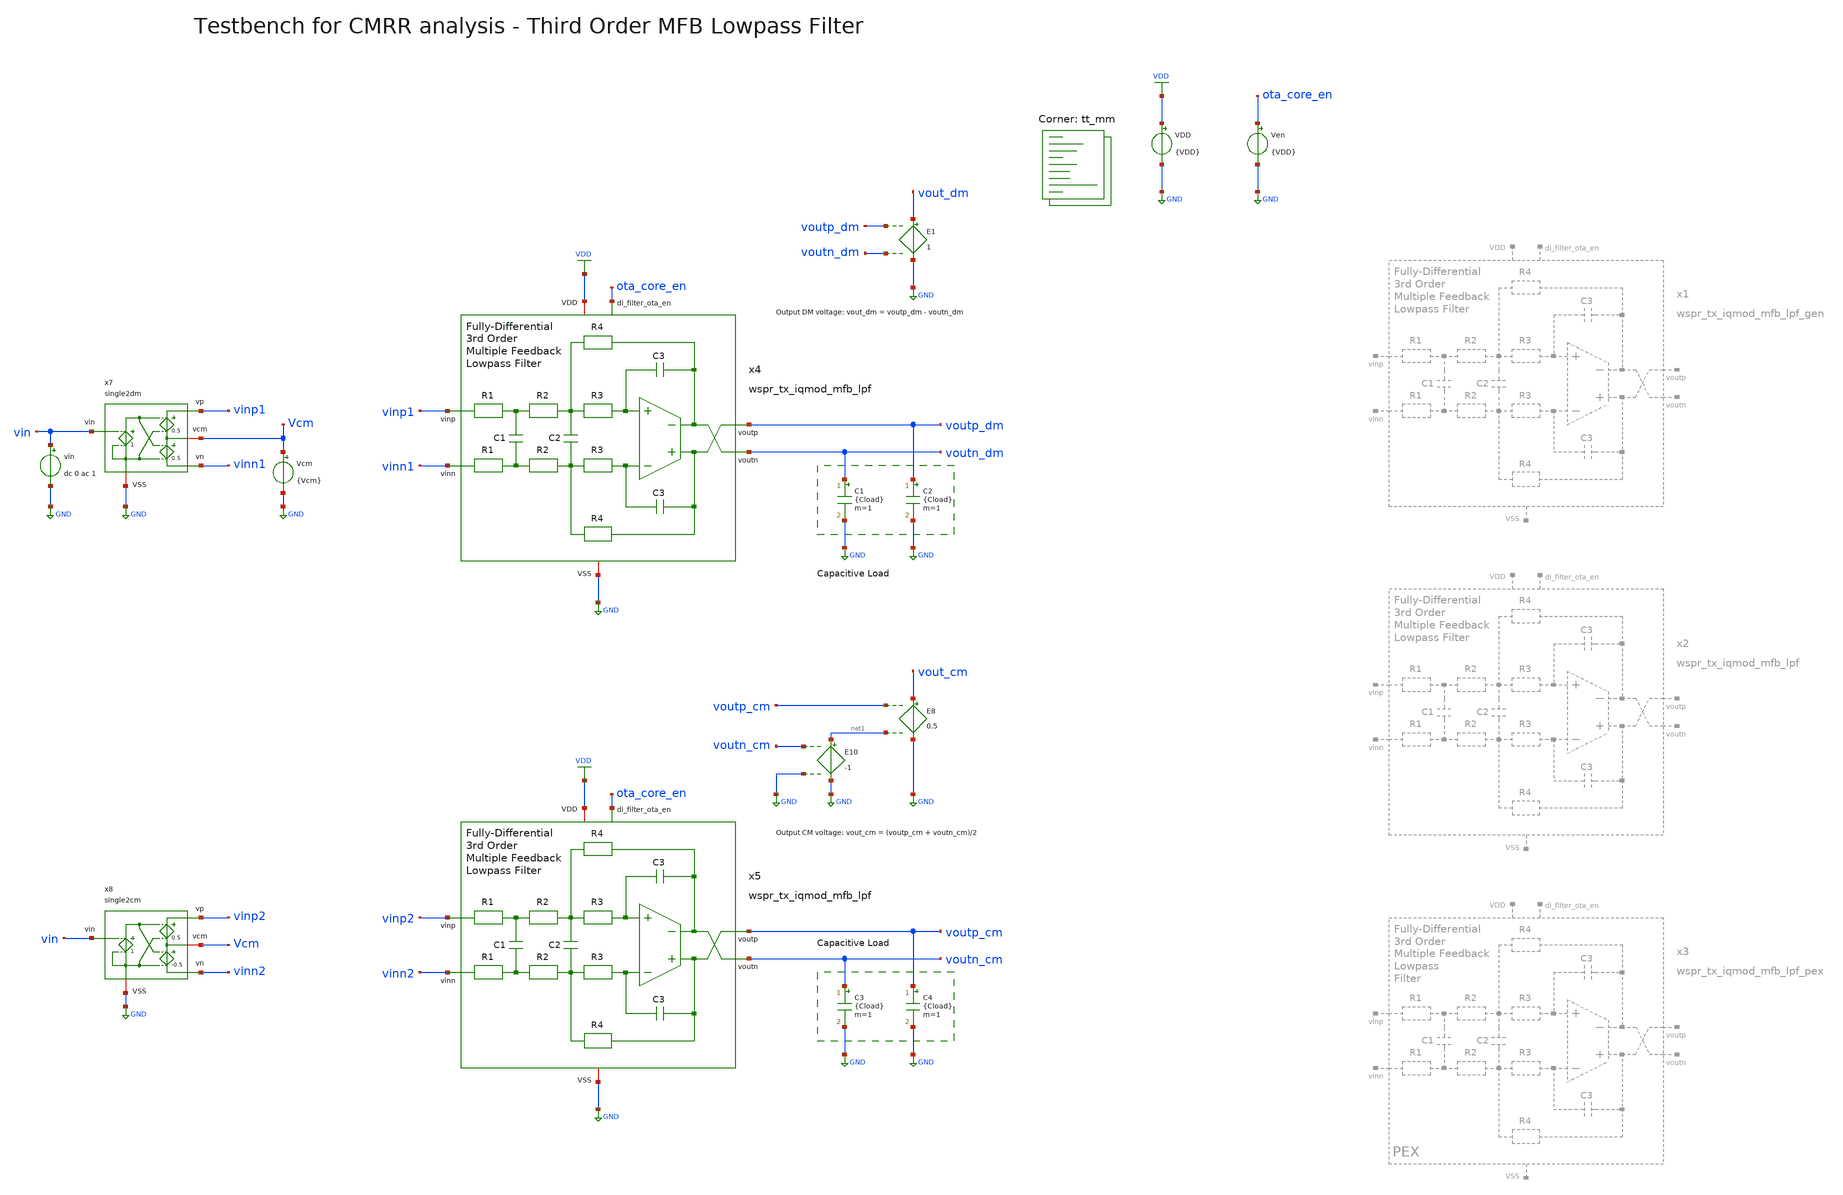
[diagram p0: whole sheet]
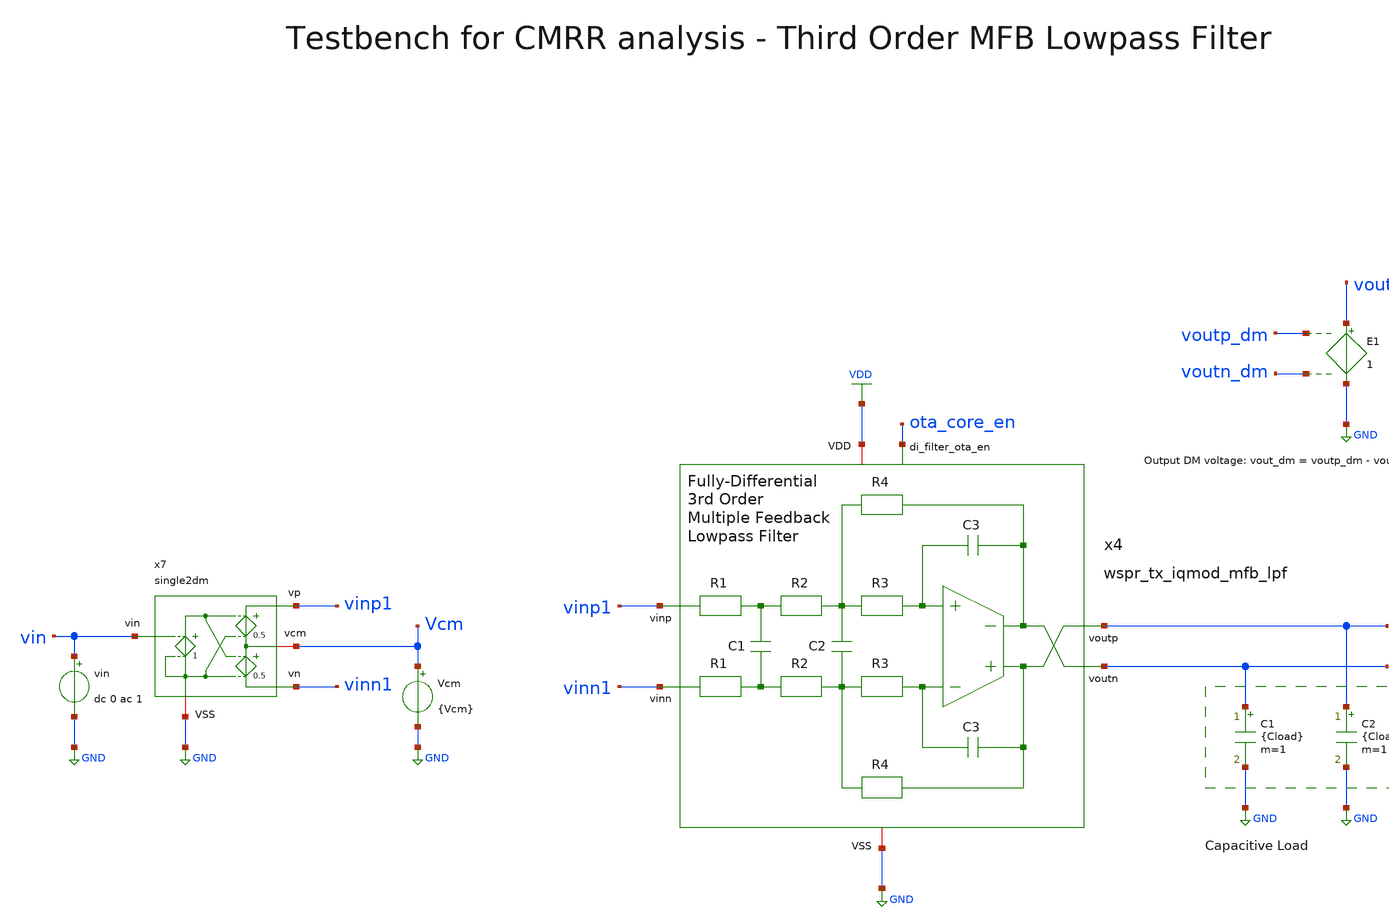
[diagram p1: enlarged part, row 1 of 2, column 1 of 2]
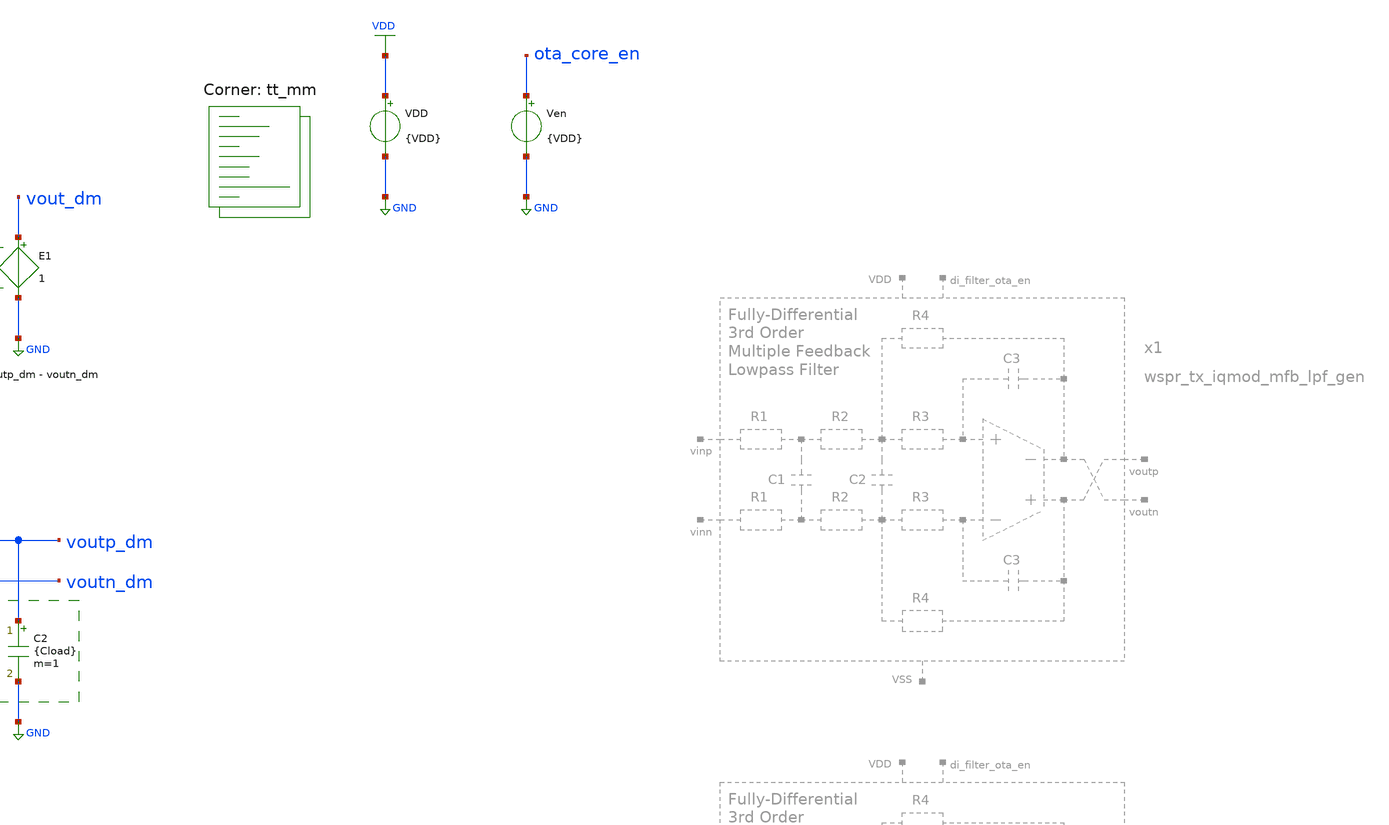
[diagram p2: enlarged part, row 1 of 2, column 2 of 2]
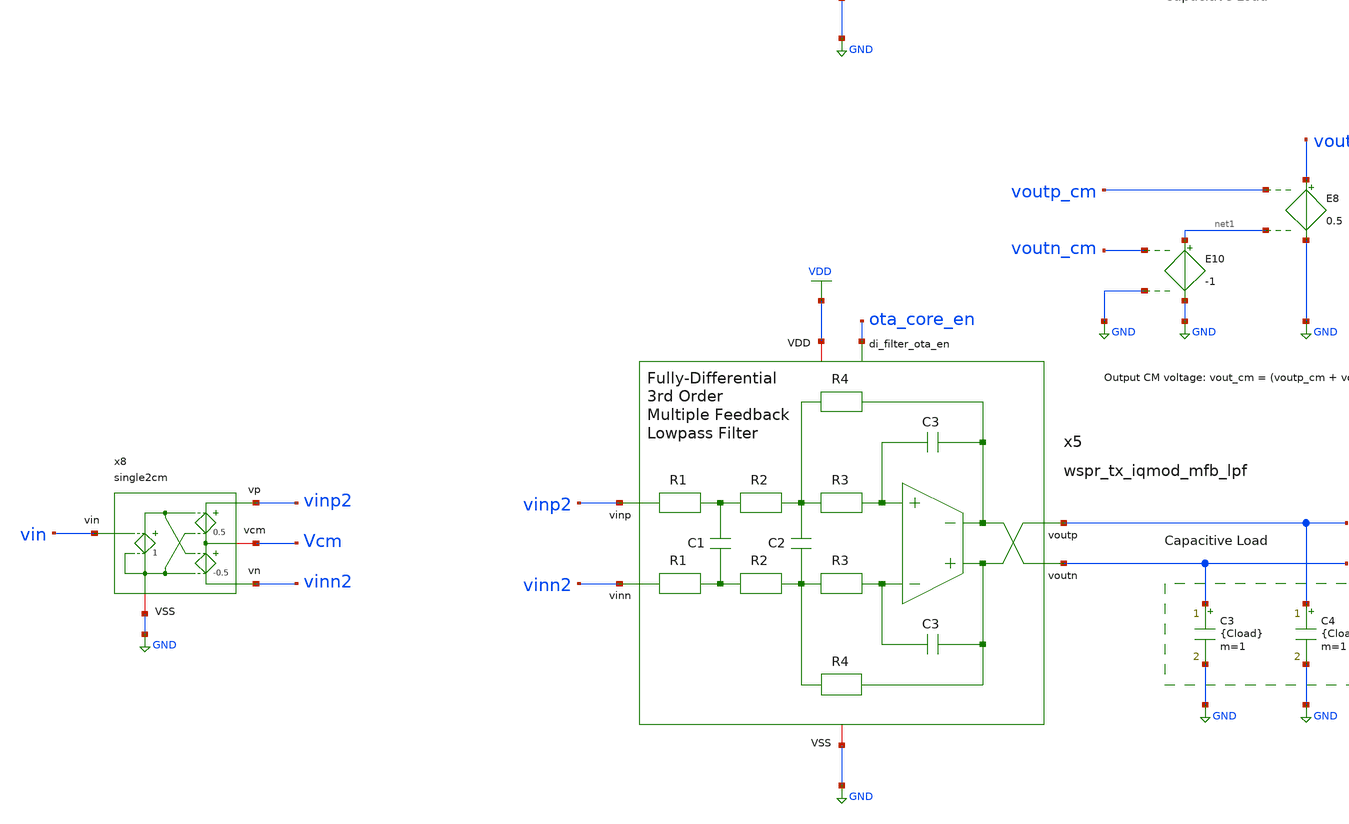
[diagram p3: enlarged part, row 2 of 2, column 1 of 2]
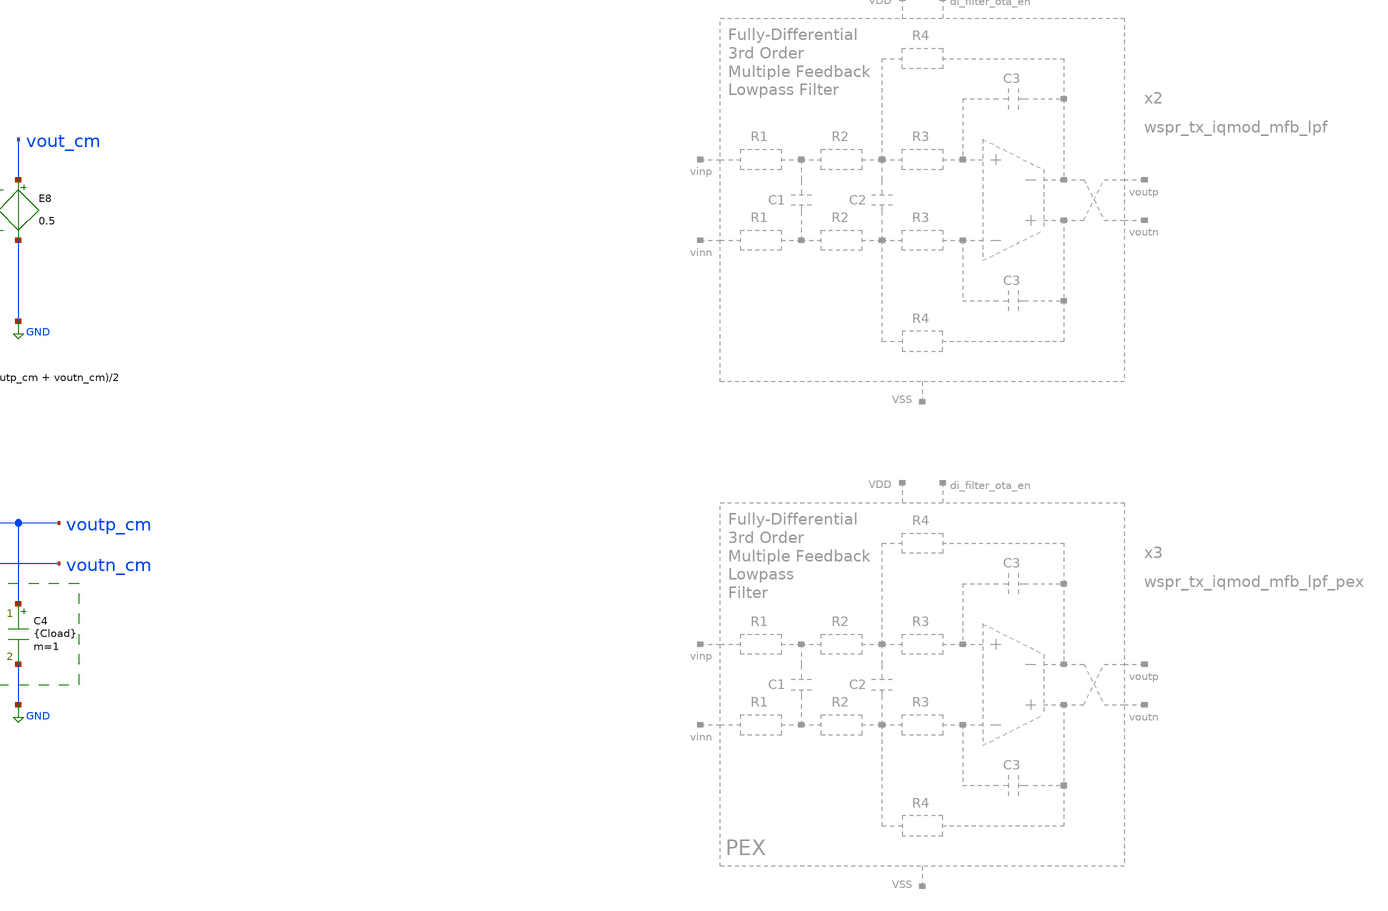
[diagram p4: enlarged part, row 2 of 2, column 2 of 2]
** sch_path: sky130/macros/iqmod/testbenches/wspr_tx_iqmod_mfb_lpf_tb_CMRR.sch
**.subckt wspr_tx_iqmod_mfb_lpf_tb_CMRR
x4 ota_core_en voutp_dm vinp1 voutn_dm vinn1 VDD GND wspr_tx_iqmod_mfb_lpf
C1 voutn_dm GND {Cload} m=1
C2 voutp_dm GND {Cload} m=1
Vcm Vcm GND {Vcm}
E1 vout_dm GND voutp_dm voutn_dm 1
vin vin GND dc 0 ac 1
C3 voutn_cm GND {Cload} m=1
C4 voutp_cm GND {Cload} m=1
E8 vout_cm GND voutp_cm net1 0.5
E10 net1 GND voutn_cm GND -1
x7 vinp1 vin Vcm GND vinn1 single2dm
x8 vinp2 vin Vcm GND vinn2 single2cm
VDD VDD GND {VDD}
Ven ota_core_en GND {VDD}
x5 ota_core_en voutp_cm vinp2 voutn_cm vinn2 VDD GND wspr_tx_iqmod_mfb_lpf
**** begin user architecture code


*.include ../../spice/wspr_tx_iqmod_mfb_lpf_pex.spice
.param VDD=1.8
.param Vcm=VDD/2
.param temp=27
.param Cload=10p
*.param W_long=18.0
*.param W_short=12.0
*.param a=3
*.param L=1.0
*.param NF_long=6
*.param NF_short=4
.param vphi=0.5
.param f_min = 10m
.csparam f_min = f_min
.param f_max = 1G
.csparam f_max = f_max
.param fdc = 10
.csparam fdc = fdc
.options savecurrents klu method=gear reltol=1e-4 abstol=1e-15 gmin=1e-15
.control

* save v(vout_dm) v(vout_cm) v(vin)
save all

set wr_vecnames
set wr_singlescale

* User Constants
let f_min = 0.1
let f_max = 1G
let fdc = 1

* Operating Point Analysis
op
remzerovec
write wspr_tx_iqmod_mfb_lpf_tb_CMRR.raw
set appendwrite

* AC Analysis
ac dec 101 $&const.f_min $&const.f_max
remzerovec
write wspr_tx_iqmod_mfb_lpf_tb_CMRR.raw

* Plotting Differential Mode Gain
let Adm = v(vout_dm)/v(vin)
let Adm_dB = vdb(Adm)
let Adm_arg = 180/PI*cphase(Adm)
plot Adm_dB Adm_arg ylabel 'Magnitude, Phase'

* Plotting Common Mode Gain
let Acm = v(vout_cm)/v(vin)
let Acm_dB = vdb(Acm)
let Acm_arg = 180/PI*cphase(Acm)
plot Acm_dB Acm_arg ylabel 'Magnitude, Phase'

* Plotting Common Mode Rejection Ratio
* let CMRR = v(vout_dm)/v(vout_cm)
let CMRR = v(Adm)/v(Acm)
let CMRR_dB = vdb(CMRR)
* let CMRR_dB = Adm_dB - Acm_dB
let CMRR_arg = 180/PI*cphase(CMRR)
plot CMRR_dB CMRR_arg ylabel 'Magnitude, Phase'

* Measurements
meas ac CMRRdc_dB find CMRR_dB when frequency = fdc
print CMRRdc_dB

* Write Data
unset appendwrite
set wr_vecnames
set wr_singlescale
wrdata $PROJECT_PATH/python/plot_simulations/data/wspr_tx_iqmod_mfb_lpf_tb_CMRR.txt v(Adm_dB)
+ v(Adm_arg) v(Acm_dB) v(Acm_arg) v(CMRR_dB) v(CMRR_arg)

*quit
.endc


.lib $::SKYWATER_MODELS/sky130.lib.spice tt_mm
**** end user architecture code
**.ends
.GLOBAL GND
.GLOBAL VDD
.end
